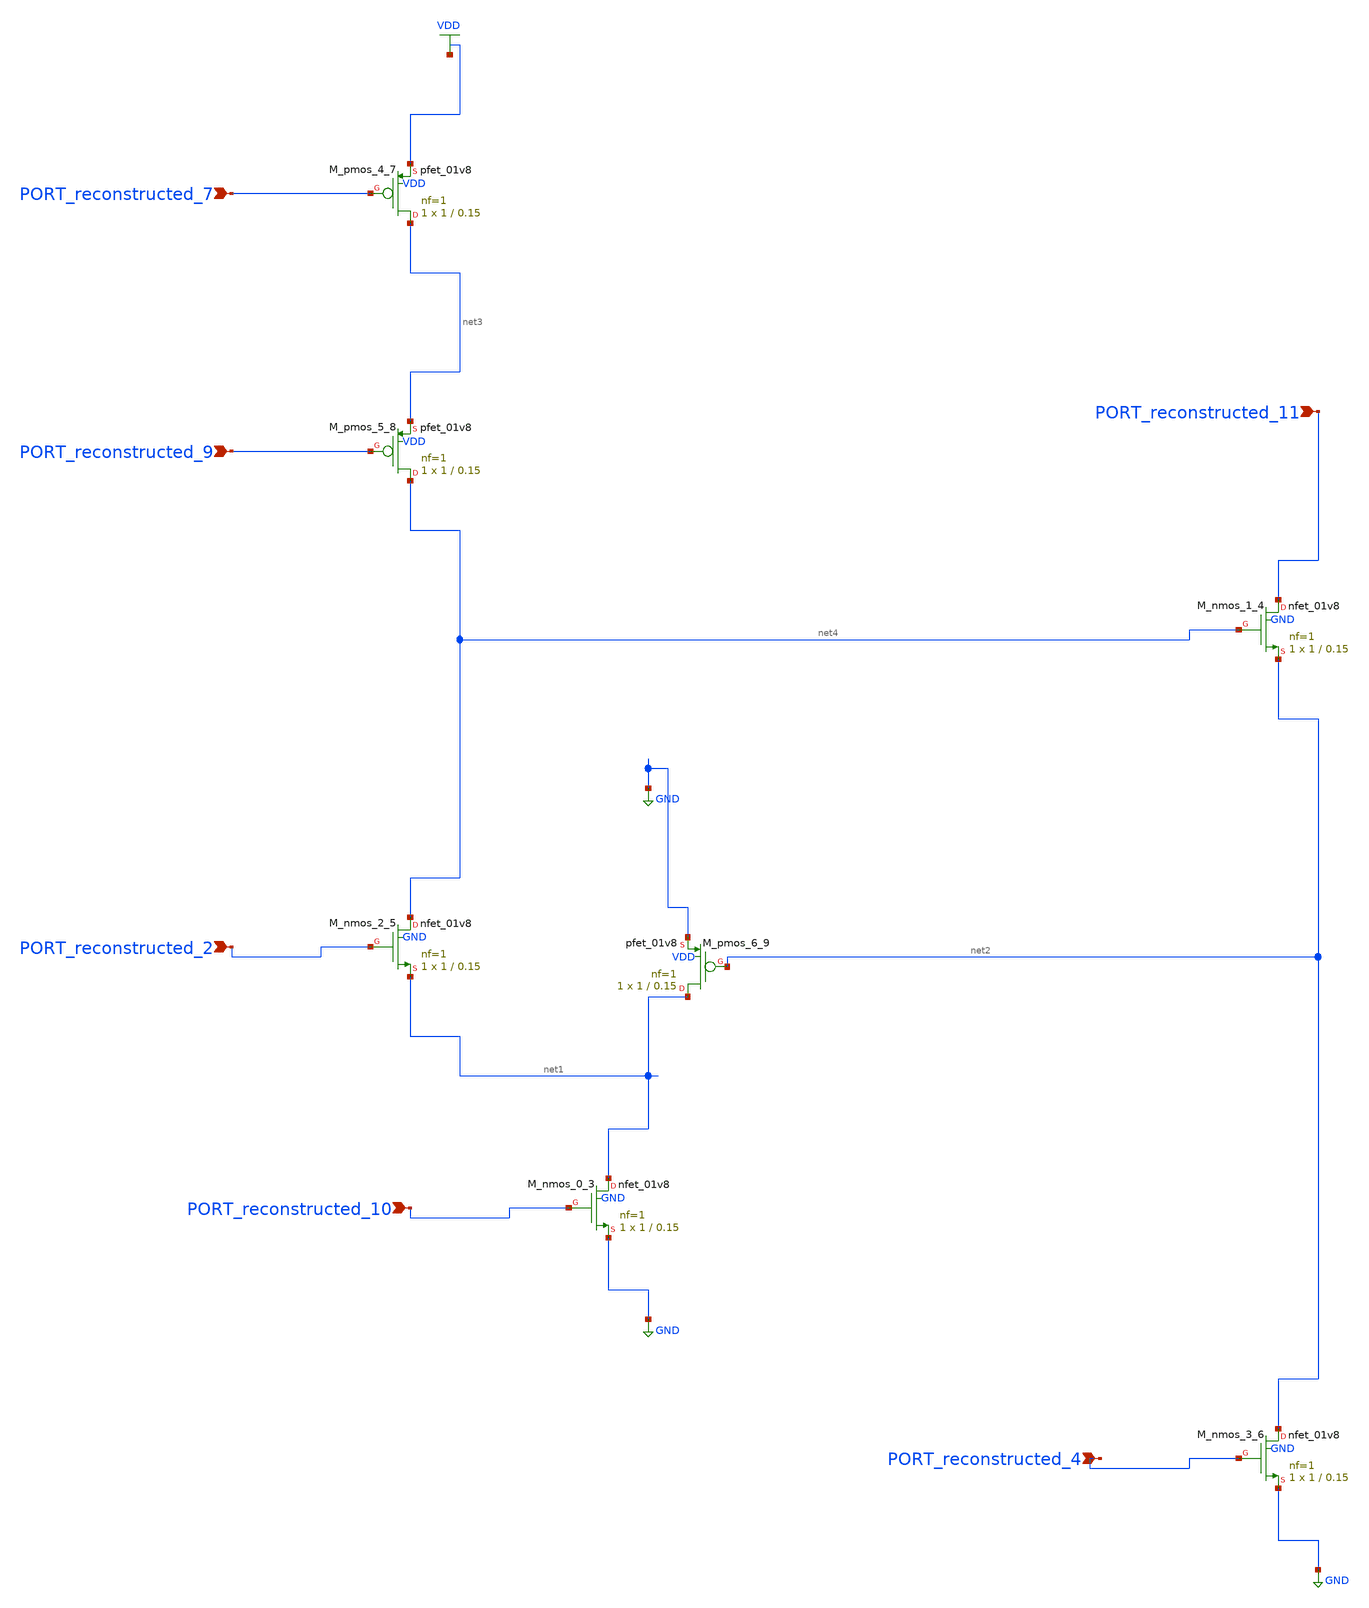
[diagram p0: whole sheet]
** sch_path: schematics/AMSNet/654.sch
**.subckt 654 PORT_reconstructed_2 PORT_reconstructed_9 PORT_reconstructed_4 PORT_reconstructed_7
*+ PORT_reconstructed_10 PORT_reconstructed_11
*.ipin PORT_reconstructed_2
*.ipin PORT_reconstructed_9
*.ipin PORT_reconstructed_4
*.ipin PORT_reconstructed_7
*.ipin PORT_reconstructed_10
*.ipin PORT_reconstructed_11
XM_nmos_0_3 net1 PORT_reconstructed_10 GND GND sky130_fd_pr__nfet_01v8 L=0.15 W=1 nf=1 ad='int((1 + 1)/2) * 1 / 1 * 0.29'
+ as='int((1 + 2)/2) * 1 / 1 * 0.29' pd='2*int((1 + 1)/2) * (1 / 1 + 0.29)' ps='2*int((1 + 2)/2) * (1 / 1 + 0.29)'
+ nrd='0.29 / 1 ' nrs='0.29 / 1 ' sa=0 sb=0 sd=0 mult=1 m=1
XM_nmos_1_4 PORT_reconstructed_11 net4 net2 GND sky130_fd_pr__nfet_01v8 L=0.15 W=1 nf=1 ad='int((1 + 1)/2) * 1 / 1 * 0.29'
+ as='int((1 + 2)/2) * 1 / 1 * 0.29' pd='2*int((1 + 1)/2) * (1 / 1 + 0.29)' ps='2*int((1 + 2)/2) * (1 / 1 + 0.29)'
+ nrd='0.29 / 1 ' nrs='0.29 / 1 ' sa=0 sb=0 sd=0 mult=1 m=1
XM_nmos_2_5 net4 PORT_reconstructed_2 net1 GND sky130_fd_pr__nfet_01v8 L=0.15 W=1 nf=1 ad='int((1 + 1)/2) * 1 / 1 * 0.29'
+ as='int((1 + 2)/2) * 1 / 1 * 0.29' pd='2*int((1 + 1)/2) * (1 / 1 + 0.29)' ps='2*int((1 + 2)/2) * (1 / 1 + 0.29)'
+ nrd='0.29 / 1 ' nrs='0.29 / 1 ' sa=0 sb=0 sd=0 mult=1 m=1
XM_nmos_3_6 net2 PORT_reconstructed_4 GND GND sky130_fd_pr__nfet_01v8 L=0.15 W=1 nf=1 ad='int((1 + 1)/2) * 1 / 1 * 0.29'
+ as='int((1 + 2)/2) * 1 / 1 * 0.29' pd='2*int((1 + 1)/2) * (1 / 1 + 0.29)' ps='2*int((1 + 2)/2) * (1 / 1 + 0.29)'
+ nrd='0.29 / 1 ' nrs='0.29 / 1 ' sa=0 sb=0 sd=0 mult=1 m=1
XM_pmos_4_7 net3 PORT_reconstructed_7 VDD VDD sky130_fd_pr__pfet_01v8 L=0.15 W=1 nf=1 ad='int((1 + 1)/2) * 1 / 1 * 0.29'
+ as='int((1 + 2)/2) * 1 / 1 * 0.29' pd='2*int((1 + 1)/2) * (1 / 1 + 0.29)' ps='2*int((1 + 2)/2) * (1 / 1 + 0.29)'
+ nrd='0.29 / 1 ' nrs='0.29 / 1 ' sa=0 sb=0 sd=0 mult=1 m=1
XM_pmos_5_8 net4 PORT_reconstructed_9 net3 VDD sky130_fd_pr__pfet_01v8 L=0.15 W=1 nf=1 ad='int((1 + 1)/2) * 1 / 1 * 0.29'
+ as='int((1 + 2)/2) * 1 / 1 * 0.29' pd='2*int((1 + 1)/2) * (1 / 1 + 0.29)' ps='2*int((1 + 2)/2) * (1 / 1 + 0.29)'
+ nrd='0.29 / 1 ' nrs='0.29 / 1 ' sa=0 sb=0 sd=0 mult=1 m=1
XM_pmos_6_9 net1 net2 GND VDD sky130_fd_pr__pfet_01v8 L=0.15 W=1 nf=1 ad='int((1 + 1)/2) * 1 / 1 * 0.29'
+ as='int((1 + 2)/2) * 1 / 1 * 0.29' pd='2*int((1 + 1)/2) * (1 / 1 + 0.29)' ps='2*int((1 + 2)/2) * (1 / 1 + 0.29)'
+ nrd='0.29 / 1 ' nrs='0.29 / 1 ' sa=0 sb=0 sd=0 mult=1 m=1
**.ends
.GLOBAL GND
.GLOBAL VDD
.end
